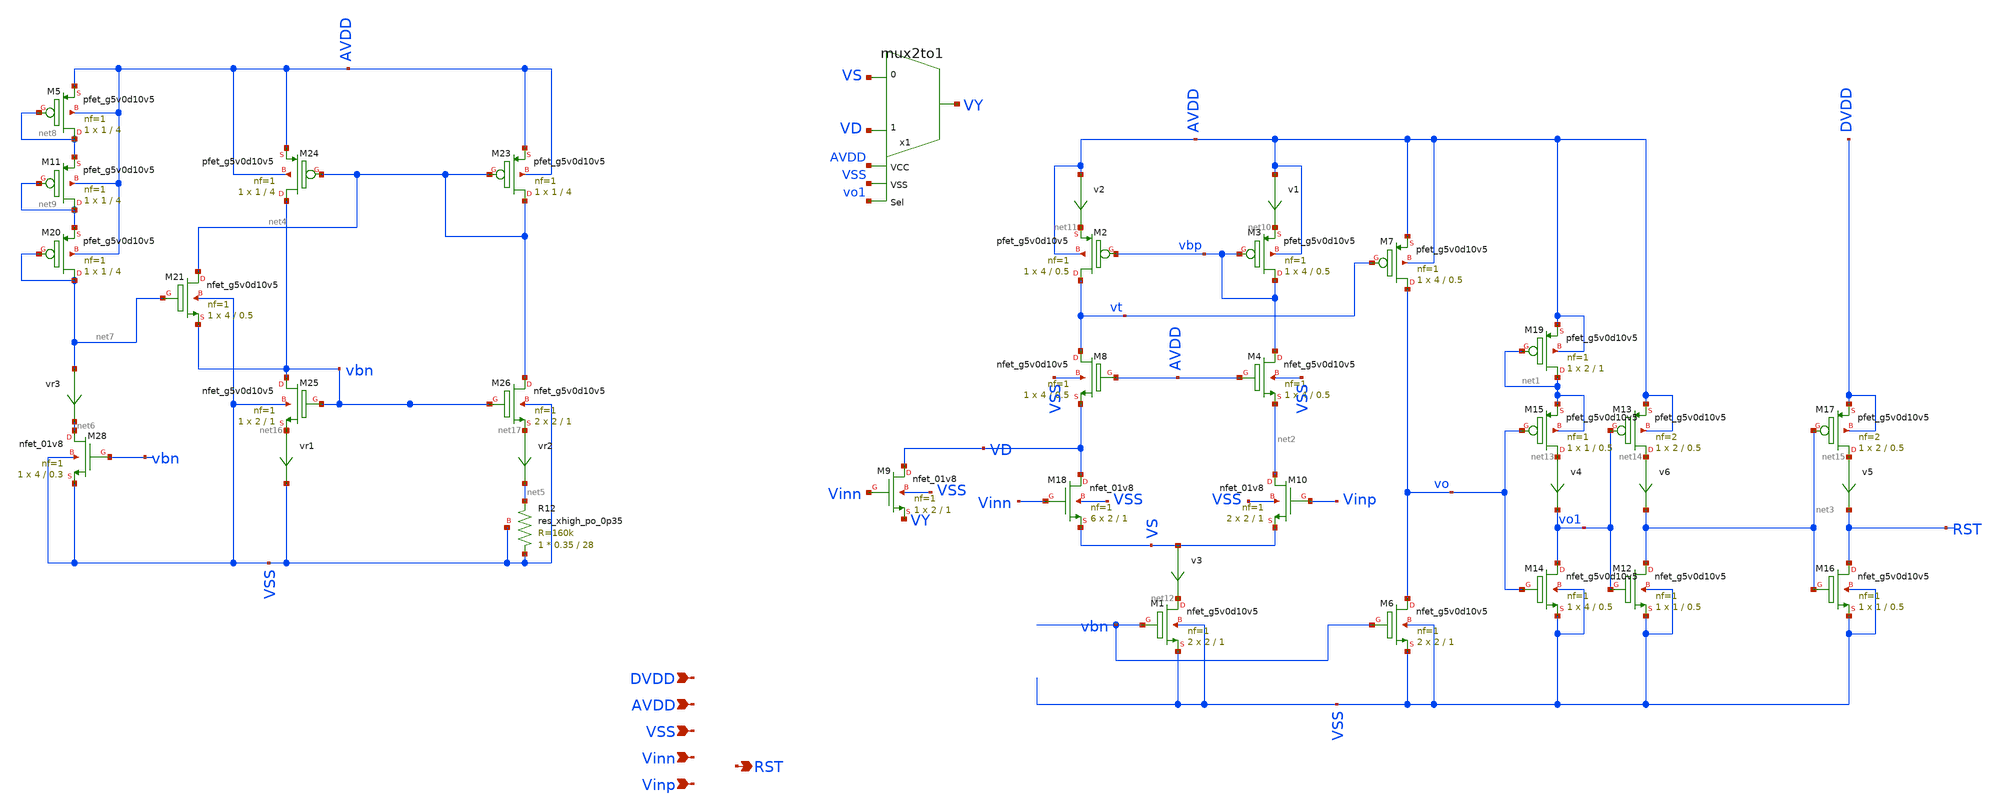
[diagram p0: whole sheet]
** sch_path: xschem/comparator_final.sch
**.subckt comparator_final AVDD RST VSS Vinn Vinp DVDD
*.ipin AVDD
*.opin RST
*.ipin VSS
*.ipin Vinn
*.ipin Vinp
*.ipin DVDD
v1 AVDD net10 0
.save i(v1)
v2 AVDD net11 0
.save i(v2)
XM1 net12 vbn VSS VSS sky130_fd_pr__nfet_g5v0d10v5 L=1 W=2 nf=1 ad='int((nf+1)/2) * W/nf * 0.29' as='int((nf+2)/2) * W/nf * 0.29'
+ pd='2*int((nf+1)/2) * (W/nf + 0.29)' ps='2*int((nf+2)/2) * (W/nf + 0.29)' nrd='0.29 / W' nrs='0.29 / W'
+ sa=0 sb=0 sd=0 mult=2 m=2
XM3 vbp vbp net10 AVDD sky130_fd_pr__pfet_g5v0d10v5 L=0.5 W=4 nf=1 ad='int((nf+1)/2) * W/nf * 0.29' as='int((nf+2)/2) * W/nf * 0.29'
+ pd='2*int((nf+1)/2) * (W/nf + 0.29)' ps='2*int((nf+2)/2) * (W/nf + 0.29)' nrd='0.29 / W' nrs='0.29 / W'
+ sa=0 sb=0 sd=0 mult=1 m=1
XM2 vt vbp net11 AVDD sky130_fd_pr__pfet_g5v0d10v5 L=0.5 W=4 nf=1 ad='int((nf+1)/2) * W/nf * 0.29' as='int((nf+2)/2) * W/nf * 0.29'
+ pd='2*int((nf+1)/2) * (W/nf + 0.29)' ps='2*int((nf+2)/2) * (W/nf + 0.29)' nrd='0.29 / W' nrs='0.29 / W'
+ sa=0 sb=0 sd=0 mult=1 m=1
v4 net13 vo1 0
.save i(v4)
XM7 vo vt AVDD AVDD sky130_fd_pr__pfet_g5v0d10v5 L=0.5 W=4 nf=1 ad='int((nf+1)/2) * W/nf * 0.29' as='int((nf+2)/2) * W/nf * 0.29'
+ pd='2*int((nf+1)/2) * (W/nf + 0.29)' ps='2*int((nf+2)/2) * (W/nf + 0.29)' nrd='0.29 / W' nrs='0.29 / W'
+ sa=0 sb=0 sd=0 mult=1 m=1
v3 VS net12 0
.save i(v3)
x1 VD VS VY AVDD VSS vo1 mux2to1
XM6 vo vbn VSS VSS sky130_fd_pr__nfet_g5v0d10v5 L=1 W=2 nf=1 ad='int((nf+1)/2) * W/nf * 0.29' as='int((nf+2)/2) * W/nf * 0.29'
+ pd='2*int((nf+1)/2) * (W/nf + 0.29)' ps='2*int((nf+2)/2) * (W/nf + 0.29)' nrd='0.29 / W' nrs='0.29 / W'
+ sa=0 sb=0 sd=0 mult=2 m=2
v6 net14 net3 0
.save i(v6)
XM14 vo1 vo VSS VSS sky130_fd_pr__nfet_g5v0d10v5 L=0.5 W=4 nf=1 ad='int((nf+1)/2) * W/nf * 0.29' as='int((nf+2)/2) * W/nf * 0.29'
+ pd='2*int((nf+1)/2) * (W/nf + 0.29)' ps='2*int((nf+2)/2) * (W/nf + 0.29)' nrd='0.29 / W' nrs='0.29 / W'
+ sa=0 sb=0 sd=0 mult=1 m=1
XM15 net13 vo net1 net1 sky130_fd_pr__pfet_g5v0d10v5 L=0.5 W=1 nf=1 ad='int((nf+1)/2) * W/nf * 0.29'
+ as='int((nf+2)/2) * W/nf * 0.29' pd='2*int((nf+1)/2) * (W/nf + 0.29)' ps='2*int((nf+2)/2) * (W/nf + 0.29)'
+ nrd='0.29 / W' nrs='0.29 / W' sa=0 sb=0 sd=0 mult=1 m=1
XM12 net3 vo1 VSS VSS sky130_fd_pr__nfet_g5v0d10v5 L=0.5 W=1 nf=1 ad='int((nf+1)/2) * W/nf * 0.29' as='int((nf+2)/2) * W/nf * 0.29'
+ pd='2*int((nf+1)/2) * (W/nf + 0.29)' ps='2*int((nf+2)/2) * (W/nf + 0.29)' nrd='0.29 / W' nrs='0.29 / W'
+ sa=0 sb=0 sd=0 mult=1 m=1
XM13 net14 vo1 AVDD AVDD sky130_fd_pr__pfet_g5v0d10v5 L=0.5 W=2 nf=2 ad='int((nf+1)/2) * W/nf * 0.29'
+ as='int((nf+2)/2) * W/nf * 0.29' pd='2*int((nf+1)/2) * (W/nf + 0.29)' ps='2*int((nf+2)/2) * (W/nf + 0.29)'
+ nrd='0.29 / W' nrs='0.29 / W' sa=0 sb=0 sd=0 mult=1 m=1
v5 net15 RST 0
.save i(v5)
XM16 RST net3 VSS VSS sky130_fd_pr__nfet_g5v0d10v5 L=0.5 W=1 nf=1 ad='int((nf+1)/2) * W/nf * 0.29' as='int((nf+2)/2) * W/nf * 0.29'
+ pd='2*int((nf+1)/2) * (W/nf + 0.29)' ps='2*int((nf+2)/2) * (W/nf + 0.29)' nrd='0.29 / W' nrs='0.29 / W'
+ sa=0 sb=0 sd=0 mult=1 m=1
XM17 net15 net3 DVDD DVDD sky130_fd_pr__pfet_g5v0d10v5 L=0.5 W=2 nf=2 ad='int((nf+1)/2) * W/nf * 0.29'
+ as='int((nf+2)/2) * W/nf * 0.29' pd='2*int((nf+1)/2) * (W/nf + 0.29)' ps='2*int((nf+2)/2) * (W/nf + 0.29)'
+ nrd='0.29 / W' nrs='0.29 / W' sa=0 sb=0 sd=0 mult=1 m=1
XM4 vbp AVDD net2 VSS sky130_fd_pr__nfet_g5v0d10v5 L=0.5 W=4 nf=1 ad='int((nf+1)/2) * W/nf * 0.29' as='int((nf+2)/2) * W/nf * 0.29'
+ pd='2*int((nf+1)/2) * (W/nf + 0.29)' ps='2*int((nf+2)/2) * (W/nf + 0.29)' nrd='0.29 / W' nrs='0.29 / W'
+ sa=0 sb=0 sd=0 mult=1 m=1
XM8 vt AVDD VD VSS sky130_fd_pr__nfet_g5v0d10v5 L=0.5 W=4 nf=1 ad='int((nf+1)/2) * W/nf * 0.29' as='int((nf+2)/2) * W/nf * 0.29'
+ pd='2*int((nf+1)/2) * (W/nf + 0.29)' ps='2*int((nf+2)/2) * (W/nf + 0.29)' nrd='0.29 / W' nrs='0.29 / W'
+ sa=0 sb=0 sd=0 mult=1 m=1
XM19 net1 net1 AVDD AVDD sky130_fd_pr__pfet_g5v0d10v5 L=1 W=2 nf=1 ad='int((nf+1)/2) * W/nf * 0.29' as='int((nf+2)/2) * W/nf * 0.29'
+ pd='2*int((nf+1)/2) * (W/nf + 0.29)' ps='2*int((nf+2)/2) * (W/nf + 0.29)' nrd='0.29 / W' nrs='0.29 / W'
+ sa=0 sb=0 sd=0 mult=1 m=1
XM23 net4 net4 AVDD AVDD sky130_fd_pr__pfet_g5v0d10v5 L=4 W=1 nf=1 ad='int((nf+1)/2) * W/nf * 0.29' as='int((nf+2)/2) * W/nf * 0.29'
+ pd='2*int((nf+1)/2) * (W/nf + 0.29)' ps='2*int((nf+2)/2) * (W/nf + 0.29)' nrd='0.29 / W' nrs='0.29 / W'
+ sa=0 sb=0 sd=0 mult=1 m=1
XM24 vbn net4 AVDD AVDD sky130_fd_pr__pfet_g5v0d10v5 L=4 W=1 nf=1 ad='int((nf+1)/2) * W/nf * 0.29' as='int((nf+2)/2) * W/nf * 0.29'
+ pd='2*int((nf+1)/2) * (W/nf + 0.29)' ps='2*int((nf+2)/2) * (W/nf + 0.29)' nrd='0.29 / W' nrs='0.29 / W'
+ sa=0 sb=0 sd=0 mult=1 m=1
XR12 VSS net5 VSS sky130_fd_pr__res_xhigh_po_0p35 L=28 mult=1 m=1
vr1 net16 VSS 0
.save i(vr1)
vr2 net17 net5 0
.save i(vr2)
vr3 net7 net6 0
.save i(vr3)
XM25 vbn vbn net16 VSS sky130_fd_pr__nfet_g5v0d10v5 L=1 W=2 nf=1 ad='int((nf+1)/2) * W/nf * 0.29' as='int((nf+2)/2) * W/nf * 0.29'
+ pd='2*int((nf+1)/2) * (W/nf + 0.29)' ps='2*int((nf+2)/2) * (W/nf + 0.29)' nrd='0.29 / W' nrs='0.29 / W'
+ sa=0 sb=0 sd=0 mult=1 m=1
XM26 net4 vbn net17 VSS sky130_fd_pr__nfet_g5v0d10v5 L=1 W=2 nf=1 ad='int((nf+1)/2) * W/nf * 0.29' as='int((nf+2)/2) * W/nf * 0.29'
+ pd='2*int((nf+1)/2) * (W/nf + 0.29)' ps='2*int((nf+2)/2) * (W/nf + 0.29)' nrd='0.29 / W' nrs='0.29 / W'
+ sa=0 sb=0 sd=0 mult=2 m=2
XM28 net6 vbn VSS VSS sky130_fd_pr__nfet_01v8 L=0.3 W=4 nf=1 ad='int((nf+1)/2) * W/nf * 0.29' as='int((nf+2)/2) * W/nf * 0.29'
+ pd='2*int((nf+1)/2) * (W/nf + 0.29)' ps='2*int((nf+2)/2) * (W/nf + 0.29)' nrd='0.29 / W' nrs='0.29 / W'
+ sa=0 sb=0 sd=0 mult=1 m=1
XM18 VD Vinn VS VSS sky130_fd_pr__nfet_01v8 L=1 W=2 nf=1 ad='int((nf+1)/2) * W/nf * 0.29' as='int((nf+2)/2) * W/nf * 0.29'
+ pd='2*int((nf+1)/2) * (W/nf + 0.29)' ps='2*int((nf+2)/2) * (W/nf + 0.29)' nrd='0.29 / W' nrs='0.29 / W'
+ sa=0 sb=0 sd=0 mult=6 m=6
XM9 VD Vinn VY VSS sky130_fd_pr__nfet_01v8 L=1 W=2 nf=1 ad='int((nf+1)/2) * W/nf * 0.29' as='int((nf+2)/2) * W/nf * 0.29'
+ pd='2*int((nf+1)/2) * (W/nf + 0.29)' ps='2*int((nf+2)/2) * (W/nf + 0.29)' nrd='0.29 / W' nrs='0.29 / W'
+ sa=0 sb=0 sd=0 mult=1 m=1
XM10 net2 Vinp VS VSS sky130_fd_pr__nfet_01v8 L=1 W=2 nf=1 ad='int((nf+1)/2) * W/nf * 0.29' as='int((nf+2)/2) * W/nf * 0.29'
+ pd='2*int((nf+1)/2) * (W/nf + 0.29)' ps='2*int((nf+2)/2) * (W/nf + 0.29)' nrd='0.29 / W' nrs='0.29 / W'
+ sa=0 sb=0 sd=0 mult=2 m=2
XM5 net8 net8 AVDD AVDD sky130_fd_pr__pfet_g5v0d10v5 L=4 W=1 nf=1 ad='int((nf+1)/2) * W/nf * 0.29' as='int((nf+2)/2) * W/nf * 0.29'
+ pd='2*int((nf+1)/2) * (W/nf + 0.29)' ps='2*int((nf+2)/2) * (W/nf + 0.29)' nrd='0.29 / W' nrs='0.29 / W'
+ sa=0 sb=0 sd=0 mult=1 m=1
XM11 net9 net9 net8 AVDD sky130_fd_pr__pfet_g5v0d10v5 L=4 W=1 nf=1 ad='int((nf+1)/2) * W/nf * 0.29' as='int((nf+2)/2) * W/nf * 0.29'
+ pd='2*int((nf+1)/2) * (W/nf + 0.29)' ps='2*int((nf+2)/2) * (W/nf + 0.29)' nrd='0.29 / W' nrs='0.29 / W'
+ sa=0 sb=0 sd=0 mult=1 m=1
XM20 net7 net7 net9 AVDD sky130_fd_pr__pfet_g5v0d10v5 L=4 W=1 nf=1 ad='int((nf+1)/2) * W/nf * 0.29' as='int((nf+2)/2) * W/nf * 0.29'
+ pd='2*int((nf+1)/2) * (W/nf + 0.29)' ps='2*int((nf+2)/2) * (W/nf + 0.29)' nrd='0.29 / W' nrs='0.29 / W'
+ sa=0 sb=0 sd=0 mult=1 m=1
XM21 net4 net7 vbn VSS sky130_fd_pr__nfet_g5v0d10v5 L=0.5 W=4 nf=1 ad='int((nf+1)/2) * W/nf * 0.29' as='int((nf+2)/2) * W/nf * 0.29'
+ pd='2*int((nf+1)/2) * (W/nf + 0.29)' ps='2*int((nf+2)/2) * (W/nf + 0.29)' nrd='0.29 / W' nrs='0.29 / W'
+ sa=0 sb=0 sd=0 mult=1 m=1
**.ends
.end
